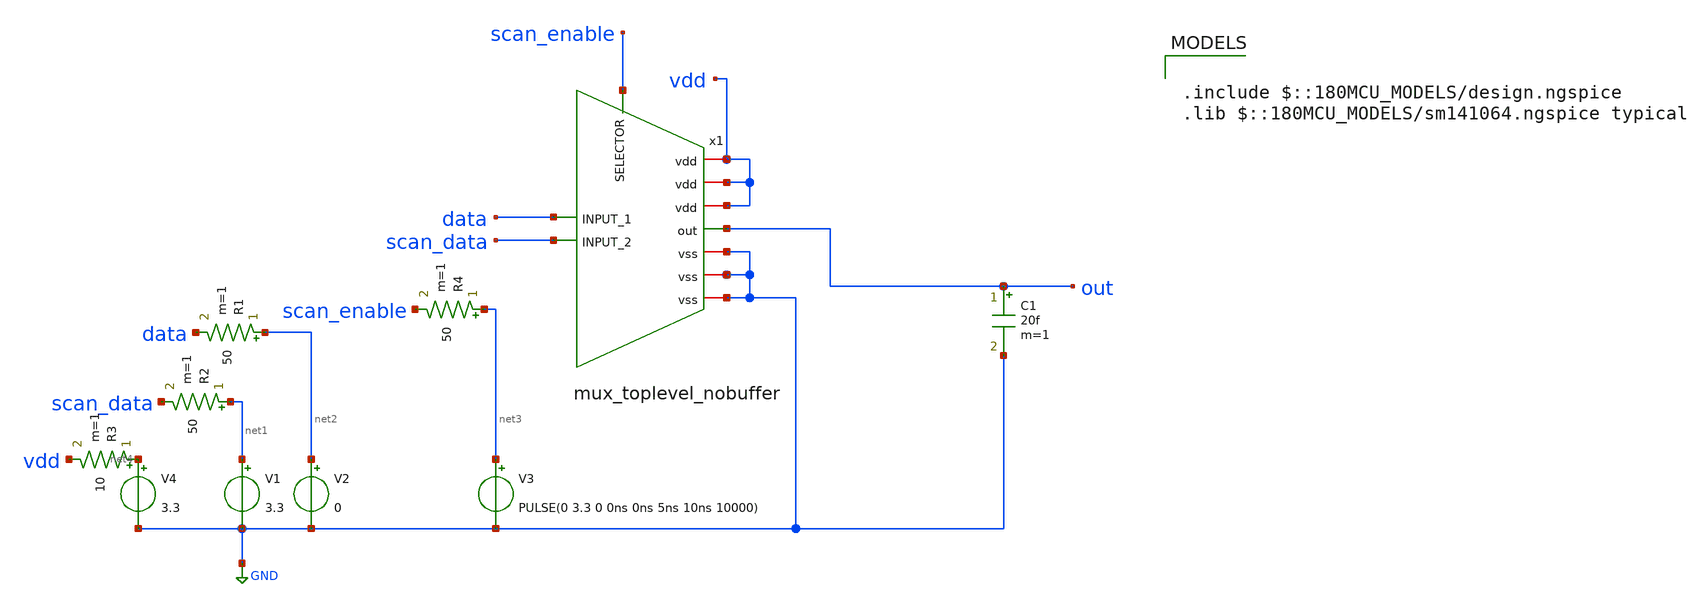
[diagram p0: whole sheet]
** sch_path: designs/libs/tb_digital/tb_mux/mux_tb.sch
**.subckt mux_tb
V1 net1 GND 3.3
V2 net2 GND 0
V3 net3 GND PULSE(0 3.3 0 0ns 0ns 5ns 10ns 10000)
V4 net4 GND 3.3
R1 net2 data 50 m=1
R2 net1 scan_data 50 m=1
R3 net4 vdd 10 m=1
R4 net3 scan_enable 50 m=1
C1 out GND 20f m=1
x1 vdd data GND out scan_data scan_enable mux_toplevel_nobuffer
**** begin user architecture code

.include $::180MCU_MODELS/design.ngspice
.lib $::180MCU_MODELS/sm141064.ngspice typical



**.include /foss/designs/voidwalkers-scandff-gf180mcu/simulation/charlib/netlist/mux_toplevel_postlayout.spice
.control
save all
tran 0.1n 1u
write mux_tb.raw
plot out

.endc


**** end user architecture code
**.ends
.GLOBAL GND
.end
